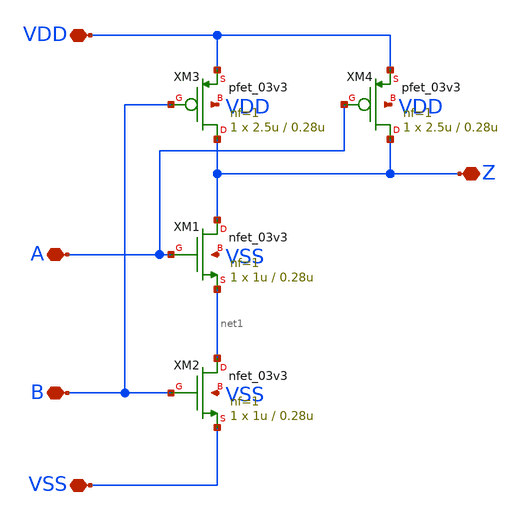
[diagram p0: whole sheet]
** sch_path: designs/comparator/nand.sch
**.subckt nand VDD VSS Z A B
*.iopin VDD
*.iopin VSS
*.iopin Z
*.iopin A
*.iopin B
XM1 Z A net1 VSS nfet_03v3 L=0.28u W=1u nf=1 ad='int((nf+1)/2) * W/nf * 0.18u' as='int((nf+2)/2) * W/nf * 0.18u'
+ pd='2*int((nf+1)/2) * (W/nf + 0.18u)' ps='2*int((nf+2)/2) * (W/nf + 0.18u)' nrd='0.18u / W' nrs='0.18u / W'
+ sa=0 sb=0 sd=0 m=1
XM2 net1 B VSS VSS nfet_03v3 L=0.28u W=1u nf=1 ad='int((nf+1)/2) * W/nf * 0.18u' as='int((nf+2)/2) * W/nf * 0.18u'
+ pd='2*int((nf+1)/2) * (W/nf + 0.18u)' ps='2*int((nf+2)/2) * (W/nf + 0.18u)' nrd='0.18u / W' nrs='0.18u / W'
+ sa=0 sb=0 sd=0 m=1
XM3 Z B VDD VDD pfet_03v3 L=0.28u W=2.5u nf=1 ad='int((nf+1)/2) * W/nf * 0.18u' as='int((nf+2)/2) * W/nf * 0.18u'
+ pd='2*int((nf+1)/2) * (W/nf + 0.18u)' ps='2*int((nf+2)/2) * (W/nf + 0.18u)' nrd='0.18u / W' nrs='0.18u / W'
+ sa=0 sb=0 sd=0 m=1
XM4 Z A VDD VDD pfet_03v3 L=0.28u W=2.5u nf=1 ad='int((nf+1)/2) * W/nf * 0.18u' as='int((nf+2)/2) * W/nf * 0.18u'
+ pd='2*int((nf+1)/2) * (W/nf + 0.18u)' ps='2*int((nf+2)/2) * (W/nf + 0.18u)' nrd='0.18u / W' nrs='0.18u / W'
+ sa=0 sb=0 sd=0 m=1
**.ends
.end
